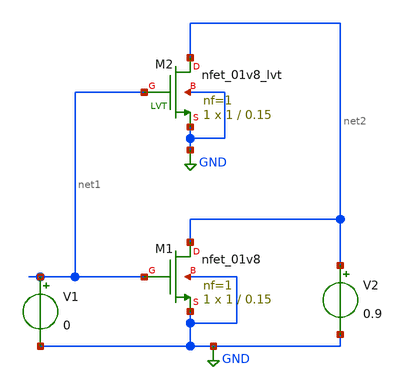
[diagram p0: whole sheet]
** sch_path: xschem_files/singeNMOS_tinyOTA.sch
**.subckt singeNMOS_tinyOTA
XM1 net2 net1 GND GND sky130_fd_pr__nfet_01v8 L=0.15 W=1 nf=1 ad='int((1 + 1)/2) * 1 / 1 * 0.29' as='int((1 + 2)/2) * 1 / 1 * 0.29'
+ pd='2*int((1 + 1)/2) * (1 / 1 + 0.29)' ps='2*int((1 + 2)/2) * (1 / 1 + 0.29)' nrd='0.29 / 1 ' nrs='0.29 / 1 '
+ sa=0 sb=0 sd=0 mult=1 m=1
V1 net1 GND 0
V2 net2 GND 0.9
XM2 net2 net1 GND GND sky130_fd_pr__nfet_01v8_lvt L=0.15 W=1 nf=1 ad='int((1 + 1)/2) * 1 / 1 * 0.29'
+ as='int((1 + 2)/2) * 1 / 1 * 0.29' pd='2*int((1 + 1)/2) * (1 / 1 + 0.29)' ps='2*int((1 + 2)/2) * (1 / 1 + 0.29)'
+ nrd='0.29 / 1 ' nrs='0.29 / 1 ' sa=0 sb=0 sd=0 mult=1 m=1
**** begin user architecture code



.lib /usr/local/share/pdk/sky130A/libs.tech/ngspice/sky130.lib.spice tt
.control
	dc V1 0 1.8 0.01
.endc


.save all


**** end user architecture code
**.ends
.GLOBAL GND
.end
